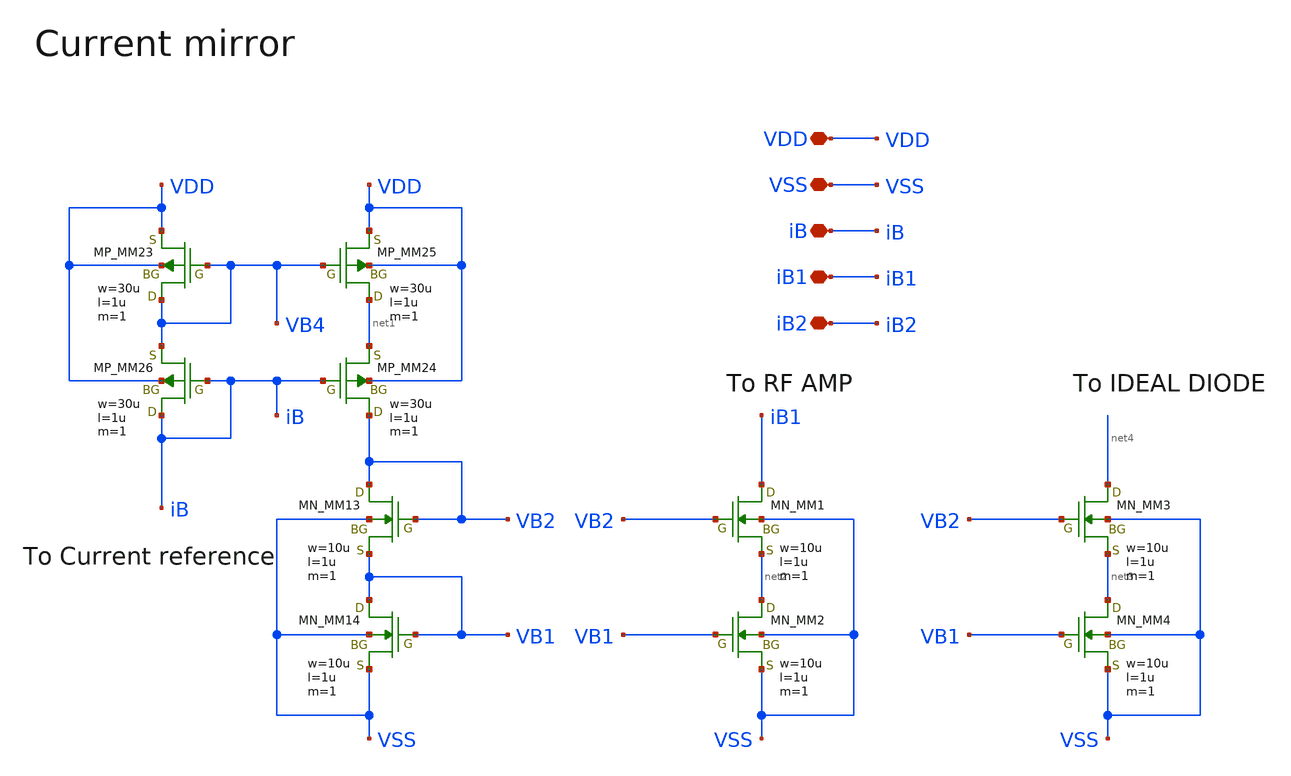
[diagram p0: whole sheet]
** sch_path: member_project/AM_Radio/Yamada3/xschem/current_mirror.sch
**.subckt current_mirror VDD VSS iB iB1 iB2
*.iopin VDD
*.iopin VSS
*.iopin iB
*.iopin iB1
*.iopin iB2
MM13 VB2 VB2 VB1 VSS NMOS w=10u l=1u as=0 ad=0 ps=0 pd=0 nrd=0 nrs=0 m=1
MM14 VB1 VB1 VSS VSS NMOS w=10u l=1u as=0 ad=0 ps=0 pd=0 nrd=0 nrs=0 m=1
MM23 VB4 VB4 VDD VDD PMOS w=30u l=1u as=0 ad=0 ps=0 pd=0 nrd=0 nrs=0 m=1
MM24 VB2 iB net1 VDD PMOS w=30u l=1u as=0 ad=0 ps=0 pd=0 nrd=0 nrs=0 m=1
MM25 net1 VB4 VDD VDD PMOS w=30u l=1u as=0 ad=0 ps=0 pd=0 nrd=0 nrs=0 m=1
MM26 iB iB VB4 VDD PMOS w=30u l=1u as=0 ad=0 ps=0 pd=0 nrd=0 nrs=0 m=1
MM1 iB1 VB2 net2 VSS NMOS w=10u l=1u as=0 ad=0 ps=0 pd=0 nrd=0 nrs=0 m=1
MM2 net2 VB1 VSS VSS NMOS w=10u l=1u as=0 ad=0 ps=0 pd=0 nrd=0 nrs=0 m=1
MM3 net4 VB2 net3 VSS NMOS w=10u l=1u as=0 ad=0 ps=0 pd=0 nrd=0 nrs=0 m=1
MM4 net3 VB1 VSS VSS NMOS w=10u l=1u as=0 ad=0 ps=0 pd=0 nrd=0 nrs=0 m=1
**.ends
.end
